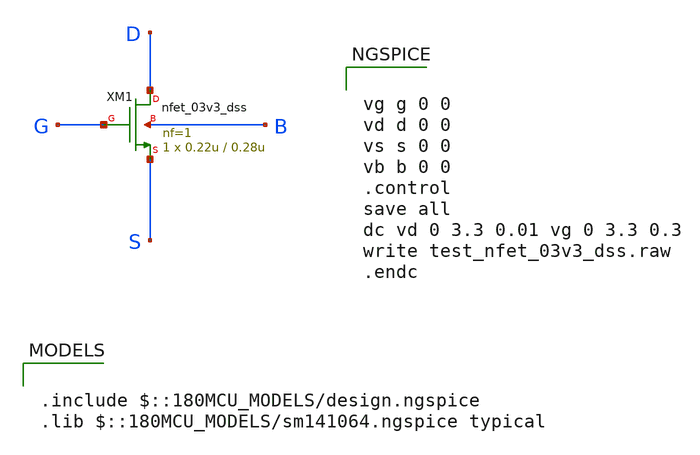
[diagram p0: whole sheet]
** sch_path: gf180mcuD/xschem_libs/gf180mcu_tests/test_nfet_03v3_dss/schematic/test_nfet_03v3_dss.sch
* Copyright 2022 GlobalFoundries PDK Authors
* Licensed under the Apache License, Version 2.0 (the "License");
* you may not use this file except in compliance with the License.
* You may obtain a copy of the License at
* https://www.apache.org/licenses/LICENSE-2.0
* Unless required by applicable law or agreed to in writing, software
* distributed under the License is distributed on an "AS IS" BASIS,
* WITHOUT WARRANTIES OR CONDITIONS OF ANY KIND, either express or implied.
* See the License for the specific language governing permissions and
* limitations under the License.
**.subckt test_nfet_03v3_dss
XM1 D G S B nfet_03v3_dss L=0.28u W=0.22u nf=1 ad='int((nf+1)/2) * W/nf * 0.18u' as='int((nf+2)/2) * W/nf * 0.18u'
+ pd='2*int((nf+1)/2) * (W/nf + 0.18u)' ps='2*int((nf+2)/2) * (W/nf + 0.18u)' nrd='0.18u / W' nrs='0.18u / W'
+ sa=0 sb=0 sd=0 d_sab=3.78u s_sab=0.28u m=1
**** begin user architecture code

.include $::180MCU_MODELS/design.ngspice
.lib $::180MCU_MODELS/sm141064.ngspice typical



vg g 0 0
vd d 0 0
vs s 0 0
vb b 0 0
.control
save all
dc vd 0 3.3 0.01 vg 0 3.3 0.3
write test_nfet_03v3_dss.raw
.endc


**** end user architecture code
**.ends
.end
